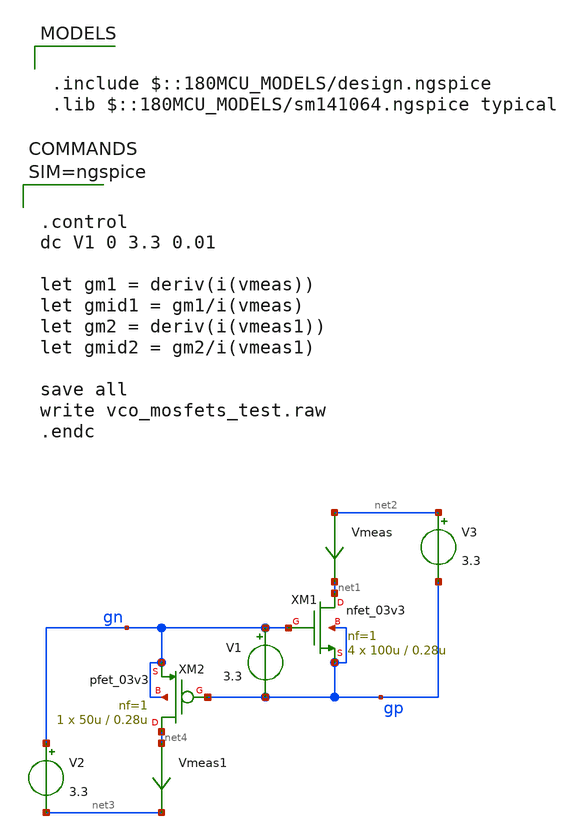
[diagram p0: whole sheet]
** sch_path: team_src/xschem/vco_mosfets_test.sch
**.subckt vco_mosfets_test
XM1 net1 gn gp gp nfet_03v3 L=0.28u W=100u nf=1 ad='int((nf+1)/2) * W/nf * 0.18u' as='int((nf+2)/2) * W/nf * 0.18u'
+ pd='2*int((nf+1)/2) * (W/nf + 0.18u)' ps='2*int((nf+2)/2) * (W/nf + 0.18u)' nrd='0.18u / W' nrs='0.18u / W'
+ sa=0 sb=0 sd=0 m=4
XM2 net4 gp gn gn pfet_03v3 L=0.28u W=50u nf=1 ad='int((nf+1)/2) * W/nf * 0.18u' as='int((nf+2)/2) * W/nf * 0.18u'
+ pd='2*int((nf+1)/2) * (W/nf + 0.18u)' ps='2*int((nf+2)/2) * (W/nf + 0.18u)' nrd='0.18u / W' nrs='0.18u / W'
+ sa=0 sb=0 sd=0 m=1
V1 gn gp 3.3
V3 net2 gp 3.3
Vmeas net2 net1 0
.save i(vmeas)
Vmeas1 net4 net3 0
.save i(vmeas1)
V2 gn net3 3.3
**** begin user architecture code



.control
dc V1 0 3.3 0.01

let gm1 = deriv(i(vmeas))
let gmid1 = gm1/i(vmeas)
let gm2 = deriv(i(vmeas1))
let gmid2 = gm2/i(vmeas1)

save all
write vco_mosfets_test.raw
.endc




.include $::180MCU_MODELS/design.ngspice
.lib $::180MCU_MODELS/sm141064.ngspice typical

**** end user architecture code
**.ends
.end
